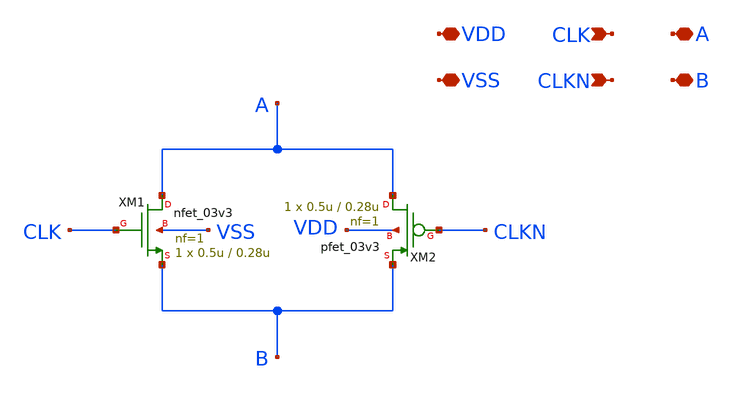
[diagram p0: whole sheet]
** sch_path: designs/sar_adc/digital/gate_tg_x1/xschem/gate_tg_x1.sch
**.subckt gate_tg_x1 VDD VSS CLK CLKN A B
*.iopin VDD
*.iopin VSS
*.ipin CLK
*.ipin CLKN
*.iopin A
*.iopin B
XM1 A CLK B VSS nfet_03v3 L=0.28u W=0.5u nf=1 ad='int((nf+1)/2) * W/nf * 0.18u' as='int((nf+2)/2) * W/nf * 0.18u'
+ pd='2*int((nf+1)/2) * (W/nf + 0.18u)' ps='2*int((nf+2)/2) * (W/nf + 0.18u)' nrd='0.18u / W' nrs='0.18u / W'
+ sa=0 sb=0 sd=0 m=1
XM2 A CLKN B VDD pfet_03v3 L=0.28u W=0.5u nf=1 ad='int((nf+1)/2) * W/nf * 0.18u' as='int((nf+2)/2) * W/nf * 0.18u'
+ pd='2*int((nf+1)/2) * (W/nf + 0.18u)' ps='2*int((nf+2)/2) * (W/nf + 0.18u)' nrd='0.18u / W' nrs='0.18u / W'
+ sa=0 sb=0 sd=0 m=1
**.ends
.end
